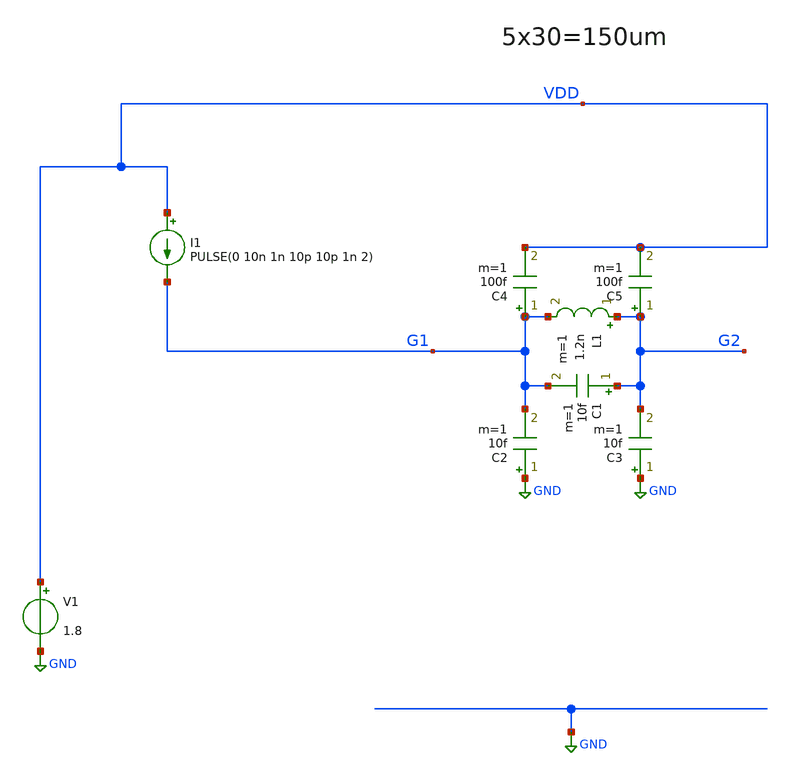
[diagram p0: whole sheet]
** sch_path: xschem/OSC_LF1_PEX.sch
**.subckt OSC_LF1_PEX
V1 VDD GND 1.8
I1 VDD G1 PULSE(0 10n 1n 10p 10p 1n 2)
C1 G2 G1 10f m=1
C2 GND G1 10f m=1
C3 GND G2 10f m=1
L1 G2 G1 1.2n m=1
C4 G1 VDD 100f m=1
C5 G2 VDD 100f m=1
**** begin user architecture code
.lib $::SKYWATER_MODELS/sky130.lib.spice ff
* .include $::PDKPATH/libs.ref/sky130_fd_sc_hvl/spice/sky130_fd_sc_hvl.spice



* .subckt sky130_fd_pr__rf_nfet_01v8_bM04W5p00L0p15_ext DRAIN GATE SOURCE SUBSTRATE
* X0 DRAIN GATE SOURCE SUBSTRATE sky130_fd_pr__nfet_01v8 ad=2.828e+12p pd=2.132e+07u as=4.242e+12p
*+ ps=3.198e+07u w=5.05e+06u l=150000u
* X1 SOURCE SUBSTRATE SUBSTRATE SUBSTRATE sky130_fd_pr__nfet_01v8 ad=0p pd=0u as=3.03e+12p
*+ ps=2.14e+07u w=5.05e+06u l=150000u
* X2 SOURCE GATE DRAIN SUBSTRATE sky130_fd_pr__nfet_01v8 ad=0p pd=0u as=0p ps=0u w=5.05e+06u
*+ l=150000u
* X3 DRAIN GATE SOURCE SUBSTRATE sky130_fd_pr__nfet_01v8 ad=0p pd=0u as=0p ps=0u w=5.05e+06u
*+ l=150000u
* X4 SUBSTRATE SUBSTRATE SOURCE SUBSTRATE sky130_fd_pr__nfet_01v8 ad=0p pd=0u as=0p ps=0u
*+ w=5.05e+06u l=150000u
* X5 SOURCE GATE DRAIN SUBSTRATE sky130_fd_pr__nfet_01v8 ad=0p pd=0u as=0p ps=0u w=5.05e+06u
*+ l=150000u
* .ends


.subckt XCP VH VL G1 G2


.subckt sky130_fd_pr__rf_pfet_01v8_aF04W5p00L0p15 DRAIN GATE SOURCE
X0 DRAIN GATE SOURCE SOURCE sky130_fd_pr__pfet_01v8 ad=2.8e+12p pd=2.112e+07u as=4.05e+12p
+ ps=3.162e+07u w=5e+06u l=150000u
X1 SOURCE GATE DRAIN SOURCE sky130_fd_pr__pfet_01v8 ad=0p pd=0u as=0p ps=0u w=5e+06u l=150000u
X2 SOURCE GATE DRAIN SOURCE sky130_fd_pr__pfet_01v8 ad=0p pd=0u as=0p ps=0u w=5e+06u l=150000u
X3 DRAIN GATE SOURCE SOURCE sky130_fd_pr__pfet_01v8 ad=0p pd=0u as=0p ps=0u w=5e+06u l=150000u
C0 DRAIN SOURCE 6.07fF
.ends



X0 VL G1 G2 VL sky130_fd_pr__nfet_01v8 ad=0p pd=0u as=0p ps=0u w=5.05e+06u l=150000u
X1 VL G1 G2 VL sky130_fd_pr__nfet_01v8 ad=0p pd=0u as=0p ps=0u w=5.05e+06u l=150000u
X2 G2 G1 VL VL sky130_fd_pr__nfet_01v8 ad=0p pd=0u as=0p ps=0u w=5.05e+06u l=150000u
X3 G2 G1 VL VL sky130_fd_pr__nfet_01v8 ad=0p pd=0u as=0p ps=0u w=5.05e+06u l=150000u
X4 VL G1 G2 VL sky130_fd_pr__nfet_01v8 ad=0p pd=0u as=0p ps=0u w=5.05e+06u l=150000u
X5 VL G1 G2 VL sky130_fd_pr__nfet_01v8 ad=0p pd=0u as=0p ps=0u w=5.05e+06u l=150000u
X6 G2 G1 VL VL sky130_fd_pr__nfet_01v8 ad=0p pd=0u as=0p ps=0u w=5.05e+06u l=150000u
X7 G2 G1 VL VL sky130_fd_pr__nfet_01v8 ad=0p pd=0u as=0p ps=0u w=5.05e+06u l=150000u
X8 VL G1 G2 VL sky130_fd_pr__nfet_01v8 ad=0p pd=0u as=0p ps=0u w=5.05e+06u l=150000u
X9 VL G1 G2 VL sky130_fd_pr__nfet_01v8 ad=0p pd=0u as=0p ps=0u w=5.05e+06u l=150000u
X10 G2 G1 VL VL sky130_fd_pr__nfet_01v8 ad=0p pd=0u as=0p ps=0u w=5.05e+06u l=150000u
X11 G2 G1 VL VL sky130_fd_pr__nfet_01v8 ad=0p pd=0u as=0p ps=0u w=5.05e+06u l=150000u
X12 VL G2 G1 VL sky130_fd_pr__nfet_01v8 ad=0p pd=0u as=0p ps=0u w=5.05e+06u l=150000u
X13 VL G2 G1 VL sky130_fd_pr__nfet_01v8 ad=0p pd=0u as=0p ps=0u w=5.05e+06u l=150000u
X14 G1 G2 VL VL sky130_fd_pr__nfet_01v8 ad=0p pd=0u as=0p ps=0u w=5.05e+06u l=150000u
X15 G1 G2 VL VL sky130_fd_pr__nfet_01v8 ad=0p pd=0u as=0p ps=0u w=5.05e+06u l=150000u
X16 VL G2 G1 VL sky130_fd_pr__nfet_01v8 ad=0p pd=0u as=0p ps=0u w=5.05e+06u l=150000u
X17 VL G2 G1 VL sky130_fd_pr__nfet_01v8 ad=0p pd=0u as=0p ps=0u w=5.05e+06u l=150000u
X18 G1 G2 VL VL sky130_fd_pr__nfet_01v8 ad=0p pd=0u as=0p ps=0u w=5.05e+06u l=150000u
X19 G1 G2 VL VL sky130_fd_pr__nfet_01v8 ad=0p pd=0u as=0p ps=0u w=5.05e+06u l=150000u
X20 VL G2 G1 VL sky130_fd_pr__nfet_01v8 ad=0p pd=0u as=0p ps=0u w=5.05e+06u l=150000u
X21 VL G2 G1 VL sky130_fd_pr__nfet_01v8 ad=0p pd=0u as=0p ps=0u w=5.05e+06u l=150000u
X22 G1 G2 VL VL sky130_fd_pr__nfet_01v8 ad=0p pd=0u as=0p ps=0u w=5.05e+06u l=150000u
X23 G1 G2 VL VL sky130_fd_pr__nfet_01v8 ad=0p pd=0u as=0p ps=0u w=5.05e+06u l=150000u
C0 G1 VH 48.54fF
C1 VH G2 48.59fF
C2 G1 G2 16.60fF
XRF_pfet_28xW5p0L0p15_0/sky130_fd_pr__rf_pfet_01v8_aF04W5p00L0p15_0 G2 G1 VH
+ sky130_fd_pr__rf_pfet_01v8_aF04W5p00L0p15
XRF_pfet_28xW5p0L0p15_0/sky130_fd_pr__rf_pfet_01v8_aF04W5p00L0p15_1 G2 G1 VH
+ sky130_fd_pr__rf_pfet_01v8_aF04W5p00L0p15
XRF_pfet_28xW5p0L0p15_0/sky130_fd_pr__rf_pfet_01v8_aF04W5p00L0p15_2 G2 G1 VH
+ sky130_fd_pr__rf_pfet_01v8_aF04W5p00L0p15
XRF_pfet_28xW5p0L0p15_0/sky130_fd_pr__rf_pfet_01v8_aF04W5p00L0p15_3 G2 G1 VH
+ sky130_fd_pr__rf_pfet_01v8_aF04W5p00L0p15
XRF_pfet_28xW5p0L0p15_0/sky130_fd_pr__rf_pfet_01v8_aF04W5p00L0p15_4 G2 G1 VH
+ sky130_fd_pr__rf_pfet_01v8_aF04W5p00L0p15
XRF_pfet_28xW5p0L0p15_0/sky130_fd_pr__rf_pfet_01v8_aF04W5p00L0p15_5 G2 G1 VH
+ sky130_fd_pr__rf_pfet_01v8_aF04W5p00L0p15
XRF_pfet_28xW5p0L0p15_0/sky130_fd_pr__rf_pfet_01v8_aF04W5p00L0p15_6 G2 G1 VH
+ sky130_fd_pr__rf_pfet_01v8_aF04W5p00L0p15
XRF_pfet_28xW5p0L0p15_1/sky130_fd_pr__rf_pfet_01v8_aF04W5p00L0p15_0 G1 G2 VH
+ sky130_fd_pr__rf_pfet_01v8_aF04W5p00L0p15
XRF_pfet_28xW5p0L0p15_1/sky130_fd_pr__rf_pfet_01v8_aF04W5p00L0p15_1 G1 G2 VH
+ sky130_fd_pr__rf_pfet_01v8_aF04W5p00L0p15
XRF_pfet_28xW5p0L0p15_1/sky130_fd_pr__rf_pfet_01v8_aF04W5p00L0p15_2 G1 G2 VH
+ sky130_fd_pr__rf_pfet_01v8_aF04W5p00L0p15
XRF_pfet_28xW5p0L0p15_1/sky130_fd_pr__rf_pfet_01v8_aF04W5p00L0p15_3 G1 G2 VH
+ sky130_fd_pr__rf_pfet_01v8_aF04W5p00L0p15
XRF_pfet_28xW5p0L0p15_1/sky130_fd_pr__rf_pfet_01v8_aF04W5p00L0p15_4 G1 G2 VH
+ sky130_fd_pr__rf_pfet_01v8_aF04W5p00L0p15
XRF_pfet_28xW5p0L0p15_1/sky130_fd_pr__rf_pfet_01v8_aF04W5p00L0p15_5 G1 G2 VH
+ sky130_fd_pr__rf_pfet_01v8_aF04W5p00L0p15
XRF_pfet_28xW5p0L0p15_1/sky130_fd_pr__rf_pfet_01v8_aF04W5p00L0p15_6 G1 G2 VH
+ sky130_fd_pr__rf_pfet_01v8_aF04W5p00L0p15
C3 G1 VL 22.49fF
C4 G2 VL 22.37fF
C5 VH VL 25.01fF
.ends

XU_XCP VDD GND G1 G2 XCP



.options savecurrents
.tran 1ps 20ns
.control
run
display
plot v(G1)
plot v(G2)
plot @I1[i]
.endc


**** end user architecture code
**.ends
.GLOBAL GND
.end
